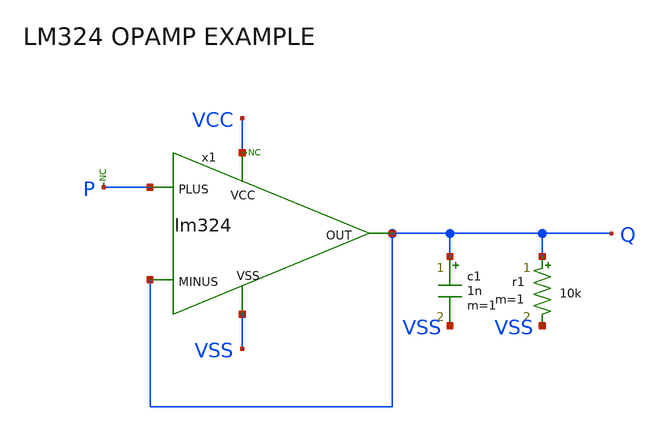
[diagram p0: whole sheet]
** sch_path: xschem_libs_newsym/examples/test_lm324/schematic/test_lm324.sch
* Copyright (C) 1998-2024 Stefan Frederik Schippers
* This program is free software; you can redistribute it and/or modify
* it under the terms of the GNU General Public License as published by
* the Free Software Foundation; either version 2 of the License, or
* (at your option) any later version.
* This program is distributed in the hope that it will be useful,
* but WITHOUT ANY WARRANTY; without even the implied warranty of
* MERCHANTABILITY or FITNESS FOR A PARTICULAR PURPOSE.  See the
* GNU General Public License for more details.
* You should have received a copy of the GNU General Public License
* along with this program; if not, write to the Free Software
**.subckt test_lm324
x1 P Q VCC VSS Q lm324
r1 Q VSS 10k m=1
c1 Q VSS 1n m=1
* noconn P
* noconn VCC
**** begin user architecture code



.option RUNLVL=5 post
.param VCC=10
.param VSS=0
.temp  25
vvcc vcc 0 dc VCC
vvss vss 0 dc VSS
vp p 0 pwl 0 0 100n 2 200u 2 201u 3 400u 3 401u 1

** models are generally not free: you must download
** SPICE models for active devices and put them  into the below
** referenced file in netlist/simulation directory.
.include model_lm324.txt
.tran 0.1u 500u


**** end user architecture code
**.ends
.end
